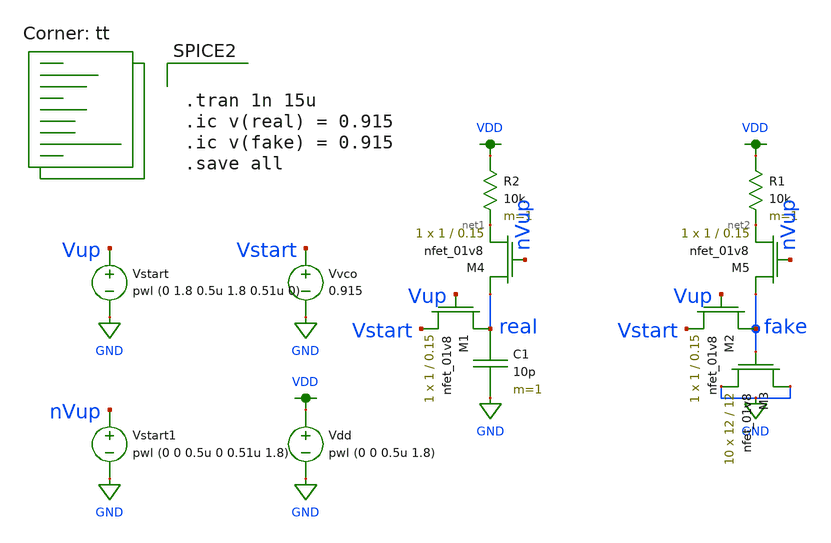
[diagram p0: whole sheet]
** sch_path: test_capacitor.sch
**.subckt test_capacitor
Vdd VDD GND pwl (0 0 0.5u 1.8)
C1 real GND 10p m=1
R2 VDD net1 10k m=1
R1 VDD net2 10k m=1
XM3 GND fake GND GND sky130_fd_pr__nfet_01v8 L=12 W=12 nf=1 ad='int((nf+1)/2) * W/nf * 0.29' as='int((nf+2)/2) * W/nf * 0.29'
+ pd='2*int((nf+1)/2) * (W/nf + 0.29)' ps='2*int((nf+2)/2) * (W/nf + 0.29)' nrd='0.29 / W' nrs='0.29 / W'
+ sa=0 sb=0 sd=0 mult=10 m=10
Vvco Vstart GND 0.915
Vstart Vup GND pwl (0 1.8 0.5u 1.8 0.51u 0)
XM1 real Vup Vstart GND sky130_fd_pr__nfet_01v8 L=0.15 W=1 nf=1 ad='int((nf+1)/2) * W/nf * 0.29' as='int((nf+2)/2) * W/nf * 0.29'
+ pd='2*int((nf+1)/2) * (W/nf + 0.29)' ps='2*int((nf+2)/2) * (W/nf + 0.29)' nrd='0.29 / W' nrs='0.29 / W'
+ sa=0 sb=0 sd=0 mult=1 m=1
XM2 fake Vup Vstart GND sky130_fd_pr__nfet_01v8 L=0.15 W=1 nf=1 ad='int((nf+1)/2) * W/nf * 0.29' as='int((nf+2)/2) * W/nf * 0.29'
+ pd='2*int((nf+1)/2) * (W/nf + 0.29)' ps='2*int((nf+2)/2) * (W/nf + 0.29)' nrd='0.29 / W' nrs='0.29 / W'
+ sa=0 sb=0 sd=0 mult=1 m=1
XM4 real nVup net1 GND sky130_fd_pr__nfet_01v8 L=0.15 W=1 nf=1 ad='int((nf+1)/2) * W/nf * 0.29' as='int((nf+2)/2) * W/nf * 0.29'
+ pd='2*int((nf+1)/2) * (W/nf + 0.29)' ps='2*int((nf+2)/2) * (W/nf + 0.29)' nrd='0.29 / W' nrs='0.29 / W'
+ sa=0 sb=0 sd=0 mult=1 m=1
XM5 fake nVup net2 GND sky130_fd_pr__nfet_01v8 L=0.15 W=1 nf=1 ad='int((nf+1)/2) * W/nf * 0.29' as='int((nf+2)/2) * W/nf * 0.29'
+ pd='2*int((nf+1)/2) * (W/nf + 0.29)' ps='2*int((nf+2)/2) * (W/nf + 0.29)' nrd='0.29 / W' nrs='0.29 / W'
+ sa=0 sb=0 sd=0 mult=1 m=1
Vstart1 nVup GND pwl (0 0 0.5u 0 0.51u 1.8)
**** begin user architecture code
.lib $::SKYWATER_MODELS/sky130.lib.spice tt


.tran 1n 15u
.ic v(real) = 0.915
.ic v(fake) = 0.915
.save all


**** end user architecture code
**.ends
.GLOBAL GND
.GLOBAL VDD
.end
